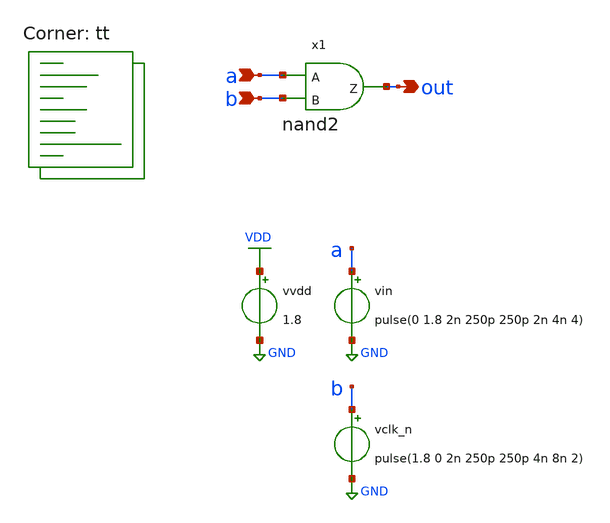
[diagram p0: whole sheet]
** sch_path: xschem/sim/tb_nand2.sch
**.subckt tb_nand2 out a b
*.opin out
*.ipin a
*.ipin b
vvdd VDD GND 1.8
vin a GND pulse(0 1.8 2n 250p 250p 2n 4n 4)
vclk_n b GND pulse(1.8 0 2n 250p 250p 4n 8n 2)
x1 a b out nand2
**** begin user architecture code
.lib $::SKYWATER_MODELS/sky130.lib.spice tt


.control
* Transient analysis
TRAN 1p 20n
save all
set filetype=binary
write tb_nand2_tran.raw
.endc


**** end user architecture code
**.ends

* expanding   symbol:  nand2.sym # of pins=3
** sym_path: xschem/nand2.sym
** sch_path: xschem/nand2.sch
.subckt nand2 A B Z
*.ipin A
*.ipin B
*.opin Z
XM1 Z A net1 GND sky130_fd_pr__nfet_01v8 L=0.15 W=0.84 nf=1 ad='int((nf+1)/2) * W/nf * 0.29' as='int((nf+2)/2) * W/nf * 0.29'
+ pd='2*int((nf+1)/2) * (W/nf + 0.29)' ps='2*int((nf+2)/2) * (W/nf + 0.29)' nrd='0.29 / W' nrs='0.29 / W'
+ sa=0 sb=0 sd=0 mult=1 m=1
XM2 net1 B GND GND sky130_fd_pr__nfet_01v8 L=0.15 W=0.84 nf=1 ad='int((nf+1)/2) * W/nf * 0.29' as='int((nf+2)/2) * W/nf * 0.29'
+ pd='2*int((nf+1)/2) * (W/nf + 0.29)' ps='2*int((nf+2)/2) * (W/nf + 0.29)' nrd='0.29 / W' nrs='0.29 / W'
+ sa=0 sb=0 sd=0 mult=1 m=1
XM3 Z B VDD VDD sky130_fd_pr__pfet_01v8 L=0.15 W=0.84 nf=1 ad='int((nf+1)/2) * W/nf * 0.29' as='int((nf+2)/2) * W/nf * 0.29'
+ pd='2*int((nf+1)/2) * (W/nf + 0.29)' ps='2*int((nf+2)/2) * (W/nf + 0.29)' nrd='0.29 / W' nrs='0.29 / W'
+ sa=0 sb=0 sd=0 mult=1 m=1
XM4 Z A VDD VDD sky130_fd_pr__pfet_01v8 L=0.15 W=0.84 nf=1 ad='int((nf+1)/2) * W/nf * 0.29' as='int((nf+2)/2) * W/nf * 0.29'
+ pd='2*int((nf+1)/2) * (W/nf + 0.29)' ps='2*int((nf+2)/2) * (W/nf + 0.29)' nrd='0.29 / W' nrs='0.29 / W'
+ sa=0 sb=0 sd=0 mult=1 m=1
.ends

.GLOBAL VDD
.GLOBAL GND
.end
